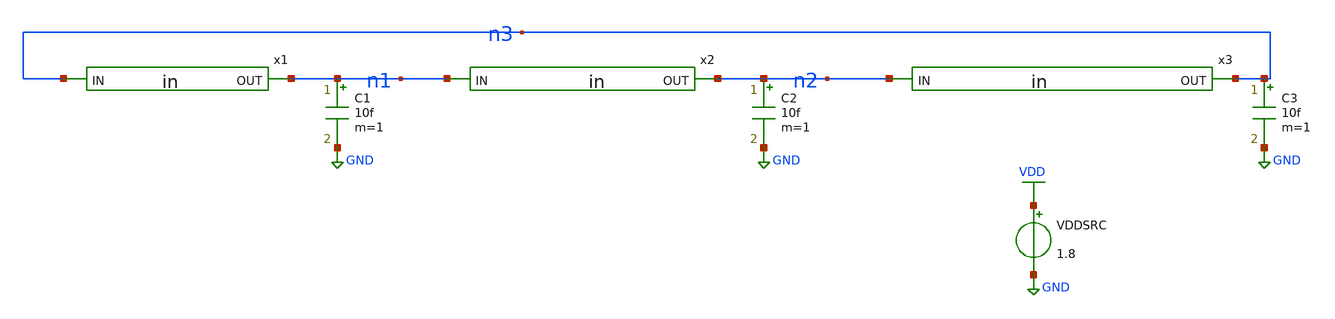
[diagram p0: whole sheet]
** sch_path: schematics/ring3_mc.sch
**.subckt ring3_mc
x1 n3 n1 in
x2 n1 n2 in
x3 n2 n3 in
VDDSRC VDD GND 1.8
C1 n1 GND 10f m=1
C2 n2 GND 10f m=1
C3 n3 GND 10f m=1
**** begin user architecture code

.lib /home/devesh/vlsi_tools/open_pdks/sky130/sky130A/libs.tech/ngspice/sky130.lib.spice fs
.param MC_PR_SWITCH=1
.param MC_MM_SWITCH=1
.ic V(n1)=1.8 V(n2)=0 V(n3)=0
.temp 27


.control

let runs = 100
let r = 0

dowhile r < runs

  echo =====================================
  echo Monte Carlo Run:
  print r

  reset
  tran 1p 10n uic

  meas tran period TRIG v(n1) VAL=0.9 RISE=5 TARG v(n1) VAL=0.9 RISE=6

  let freq = 1/period
  print period
  print freq

  let r = r + 1

end

.endc

**** end user architecture code
**.ends

* expanding   symbol:  in.sym # of pins=2
** sym_path: schematics/in.sym
** sch_path: schematics/in.sch
.subckt in IN OUT
*.opin OUT
*.ipin IN
XM1 OUT IN VDD VDD sky130_fd_pr__pfet_01v8 L=0.15 W=1 nf=1 ad='int((nf+1)/2) * W/nf * 0.29' as='int((nf+2)/2) * W/nf * 0.29'
+ pd='2*int((nf+1)/2) * (W/nf + 0.29)' ps='2*int((nf+2)/2) * (W/nf + 0.29)' nrd='0.29 / W' nrs='0.29 / W'
+ sa=0 sb=0 sd=0 mult=1 m=1
XM2 OUT IN GND GND sky130_fd_pr__nfet_01v8 L=0.15 W=0.5 nf=1 ad='int((1 + 1)/2) * 0.5 / 1 * 0.29' as='int((1 + 2)/2) * 0.5 / 1 * 0.29'
+ pd='2*int((1 + 1)/2) * (0.5 / 1 + 0.29)' ps='2*int((1 + 2)/2) * (0.5 / 1 + 0.29)' nrd='0.29 / 0.5 ' nrs='0.29 / 0.5 '
+ sa=0 sb=0 sd=0 mult=1 m=1
.ends

.GLOBAL VDD
.GLOBAL GND
.end
